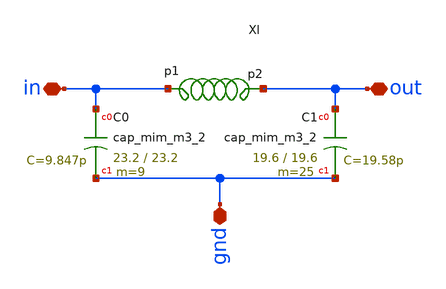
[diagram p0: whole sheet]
** sch_path: impedance-transformer/xschem/impedance-transformer.sch
**.subckt impedance-transformer gnd in out
*.iopin gnd
*.iopin in
*.iopin out
XC0 in gnd sky130_fd_pr__cap_mim_m3_2 W=23.2 L=23.2 MF=9 m=9
XC1 out gnd sky130_fd_pr__cap_mim_m3_2 W=19.6 L=19.6 MF=25 m=25
x1 in out l1
**** begin user architecture code

* NGSPICE file created from impedance-transformer.ext - technology: sky

R0 in in.t0 0.216
R1 gnd gnd.t0 0.383
R2 gnd.t1 gnd.n0 0.007
R3 gnd.t0 gnd.n3 0.004
R4 gnd.n1 gnd.t2 0.004
R5 gnd.t0 gnd.t1 0.003
R6 gnd.t0 gnd.n2 0.002
R7 gnd.t0 gnd.n1 0.001
R8 out out.t13 0.516
R9 out.n0 out.t5 0.095
R10 out.n2 out.n1 0.087
R11 out.t15 out.n2 0.087
R12 out.n1 out.n0 0.077
R13 out.t0 out.t1 0.067
R14 out.t2 out.t4 0.067
R15 out.t7 out.t10 0.067
R16 out.t10 out.t12 0.067
R17 out.t6 out.t9 0.067
R18 out.t9 out.t17 0.067
R19 out.t17 out.t2 0.067
R20 out.t2 out.t11 0.067
R21 out.t5 out.t8 0.067
R22 out.t16 out.t15 0.067
R23 out.t14 out.t16 0.067
R24 out.t3 out.t14 0.067
R25 out.t13 out.t3 0.067
R26 out.n0 out.t0 0.023
R27 out.n1 out.t7 0.023
R28 out.n2 out.t6 0.023
C0 out in 1.21fF
C1 out gnd 62.91fF
C2 out.t11 gnd 30.83fF
C3 out.t4 gnd 30.83fF
C4 out.t2 gnd 230.79fF
C5 out.t17 gnd 30.83fF
C6 out.t9 gnd 30.83fF
C7 out.t6 gnd 28.66fF
C8 out.t12 gnd 30.83fF
C9 out.t10 gnd 30.83fF
C10 out.t7 gnd 28.66fF
C11 out.t1 gnd 30.83fF
C12 out.t0 gnd 28.66fF
C13 out.t8 gnd 30.83fF
C14 out.t5 gnd 35.32fF
C15 out.n0 gnd 13.61fF $ **FLOATING
C16 out.n1 gnd 12.30fF $ **FLOATING
C17 out.n2 gnd 13.77fF $ **FLOATING
C18 out.t15 gnd 34.82fF
C19 out.t16 gnd 30.83fF
C20 out.t14 gnd 30.83fF
C21 out.t3 gnd 30.83fF
C22 out.t13 gnd 49.05fF
C23 in.t0 gnd 403.11fF
C24 in gnd 40.32fF



**** end user architecture code
**.ends

* expanding   symbol:  /home/hugodg/projects-sky130/temp-sensor/impedance-transformer/xschem/l1.sym
*+ # of pins=2
** sym_path: impedance-transformer/xschem/l1.sym
** sch_path: impedance-transformer/xschem/l1.sch
.subckt l1 p1 p2
*.iopin p2
*.iopin p1
L0 p1 net3 0.6198n m=1
Cs1 p1 net1 28.82f m=1
Cs2 p2 net2 59.62f m=1
Rs1 net1 GND 59.62 m=1
Rs2 net2 GND 17.33 m=1
R1 p2 net3 3.029 m=1
.ends

.GLOBAL GND
.end
